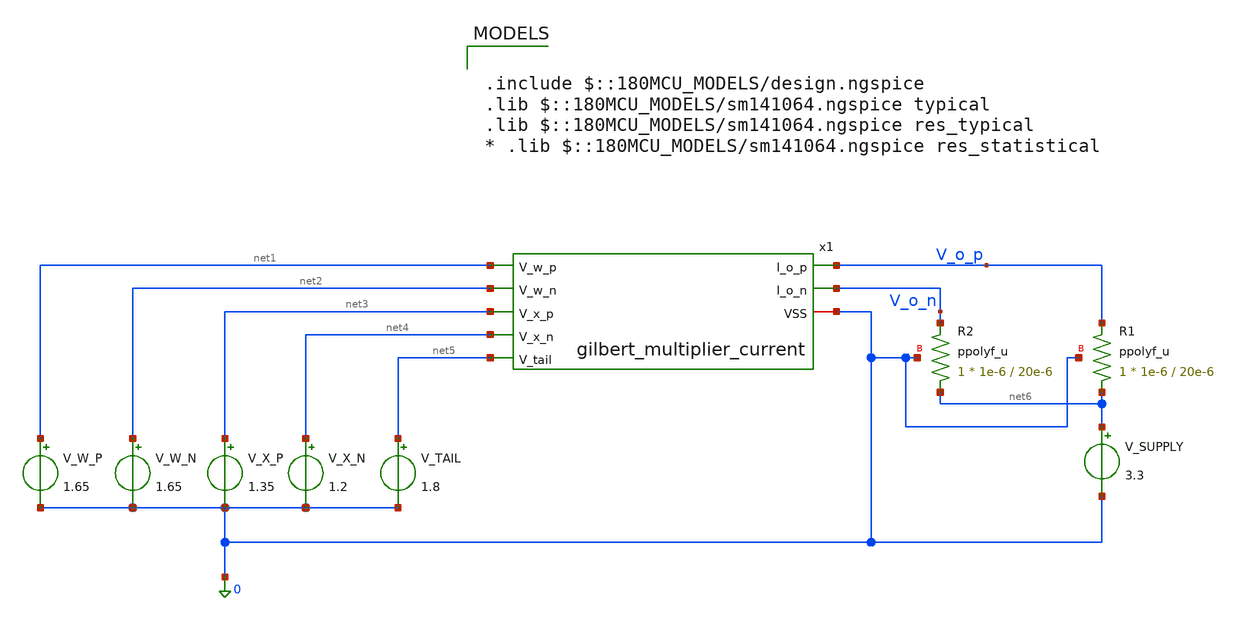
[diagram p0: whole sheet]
** sch_path: schematics/tb_gilbert_multiplier_current.sch
**.subckt tb_gilbert_multiplier_current
V_X_P net3 0 1.35
V_X_N net4 0 1.2
V_TAIL net5 0 1.8
V_W_P net1 0 1.65
V_W_N net2 0 1.65
V_SUPPLY net6 0 3.3
x1 V_o_p V_o_n net1 net2 net3 net4 net5 0 gilbert_multiplier_current
XR1 net6 V_o_p 0 ppolyf_u r_width=1e-6 r_length=20e-6 m=1
XR2 net6 V_o_n 0 ppolyf_u r_width=1e-6 r_length=20e-6 m=1
**** begin user architecture code


.control
  * Nested Sweep:
  * 1. Sweep Weight (V_W_P) from 1.15V to 2.15V in 10mV steps.
  * 2. Step Sensor (V_X_P) from 1.10V to 1.30V in 50mV steps.
  dc V_W_P 1.15 2.15 0.01 V_X_P 1.10 1.30 0.05

  * Calculate differential output
  let V_diff_out = v(V_o_p) - v(V_o_n)

  * Export the family of curves to a text file
  wrdata /foss/designs/analog-perceptron-gf180mcu/schematics/sweep_4quadrant.txt V_diff_out

  * Plot the result in the Xschem GUI
  plot V_diff_out
.endc



.include $::180MCU_MODELS/design.ngspice
.lib $::180MCU_MODELS/sm141064.ngspice typical
.lib $::180MCU_MODELS/sm141064.ngspice res_typical
* .lib $::180MCU_MODELS/sm141064.ngspice res_statistical

**** end user architecture code
**.ends

* expanding   symbol:  analog-perceptron-gf180mcu/schematics/gilbert_multiplier_current.sym # of
*+ pins=8
** sym_path: schematics/gilbert_multiplier_current.sym
** sch_path: schematics/gilbert_multiplier_current.sch
.subckt gilbert_multiplier_current I_o_p I_o_n V_w_p V_w_n V_x_p V_x_n V_tail VSS
*.ipin V_x_p
*.ipin V_x_n
*.ipin V_tail
*.iopin VSS
*.ipin V_w_p
*.ipin V_w_n
*.opin I_o_n
*.opin I_o_p
XM1 net1 V_x_p net3 VSS nfet_03v3 L=0.5u W=10u nf=1 ad='int((nf+1)/2) * W/nf * 0.18u' as='int((nf+2)/2) * W/nf * 0.18u'
+ pd='2*int((nf+1)/2) * (W/nf + 0.18u)' ps='2*int((nf+2)/2) * (W/nf + 0.18u)' nrd='0.18u / W' nrs='0.18u / W'
+ sa=0 sb=0 sd=0 m=1
XM2 net2 V_x_n net4 VSS nfet_03v3 L=0.5u W=10u nf=1 ad='int((nf+1)/2) * W/nf * 0.18u' as='int((nf+2)/2) * W/nf * 0.18u'
+ pd='2*int((nf+1)/2) * (W/nf + 0.18u)' ps='2*int((nf+2)/2) * (W/nf + 0.18u)' nrd='0.18u / W' nrs='0.18u / W'
+ sa=0 sb=0 sd=0 m=1
XM3 I_o_n V_w_p net1 VSS nfet_03v3 L=0.5u W=10u nf=1 ad='int((nf+1)/2) * W/nf * 0.18u' as='int((nf+2)/2) * W/nf * 0.18u'
+ pd='2*int((nf+1)/2) * (W/nf + 0.18u)' ps='2*int((nf+2)/2) * (W/nf + 0.18u)' nrd='0.18u / W' nrs='0.18u / W'
+ sa=0 sb=0 sd=0 m=1
XM4 I_o_p V_w_n net1 VSS nfet_03v3 L=0.5u W=10u nf=1 ad='int((nf+1)/2) * W/nf * 0.18u' as='int((nf+2)/2) * W/nf * 0.18u'
+ pd='2*int((nf+1)/2) * (W/nf + 0.18u)' ps='2*int((nf+2)/2) * (W/nf + 0.18u)' nrd='0.18u / W' nrs='0.18u / W'
+ sa=0 sb=0 sd=0 m=1
XM5 I_o_n V_w_n net2 VSS nfet_03v3 L=0.5u W=10u nf=1 ad='int((nf+1)/2) * W/nf * 0.18u' as='int((nf+2)/2) * W/nf * 0.18u'
+ pd='2*int((nf+1)/2) * (W/nf + 0.18u)' ps='2*int((nf+2)/2) * (W/nf + 0.18u)' nrd='0.18u / W' nrs='0.18u / W'
+ sa=0 sb=0 sd=0 m=1
XM6 I_o_p V_w_p net2 VSS nfet_03v3 L=0.5u W=10u nf=1 ad='int((nf+1)/2) * W/nf * 0.18u' as='int((nf+2)/2) * W/nf * 0.18u'
+ pd='2*int((nf+1)/2) * (W/nf + 0.18u)' ps='2*int((nf+2)/2) * (W/nf + 0.18u)' nrd='0.18u / W' nrs='0.18u / W'
+ sa=0 sb=0 sd=0 m=1
XM7 net3 V_tail VSS VSS nfet_03v3 L=1u W=5u nf=1 ad='int((nf+1)/2) * W/nf * 0.18u' as='int((nf+2)/2) * W/nf * 0.18u'
+ pd='2*int((nf+1)/2) * (W/nf + 0.18u)' ps='2*int((nf+2)/2) * (W/nf + 0.18u)' nrd='0.18u / W' nrs='0.18u / W'
+ sa=0 sb=0 sd=0 m=1
XM8 net4 V_tail VSS VSS nfet_03v3 L=1u W=5u nf=1 ad='int((nf+1)/2) * W/nf * 0.18u' as='int((nf+2)/2) * W/nf * 0.18u'
+ pd='2*int((nf+1)/2) * (W/nf + 0.18u)' ps='2*int((nf+2)/2) * (W/nf + 0.18u)' nrd='0.18u / W' nrs='0.18u / W'
+ sa=0 sb=0 sd=0 m=1
XR1 net3 net4 VSS ppolyf_u r_width=1e-6 r_length=40e-6 m=1
.ends

.end
